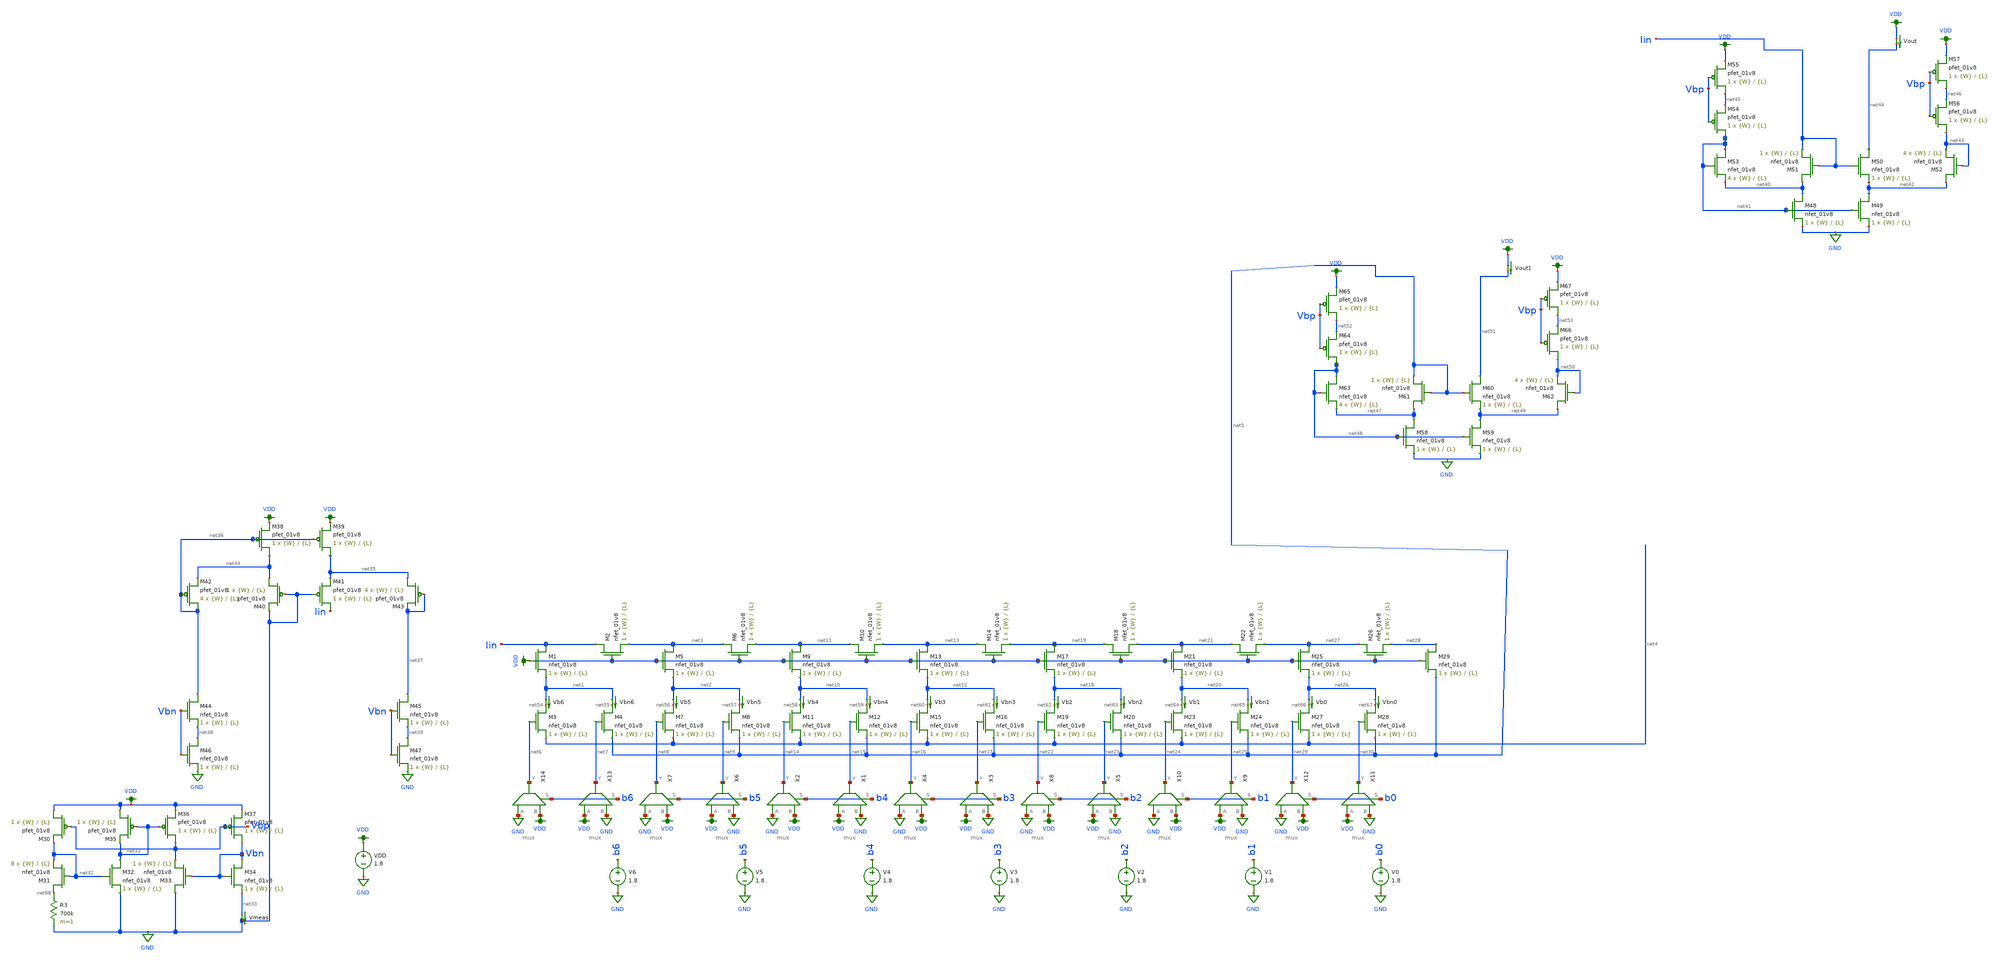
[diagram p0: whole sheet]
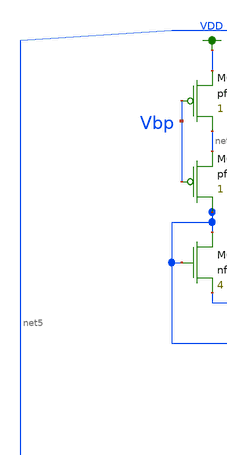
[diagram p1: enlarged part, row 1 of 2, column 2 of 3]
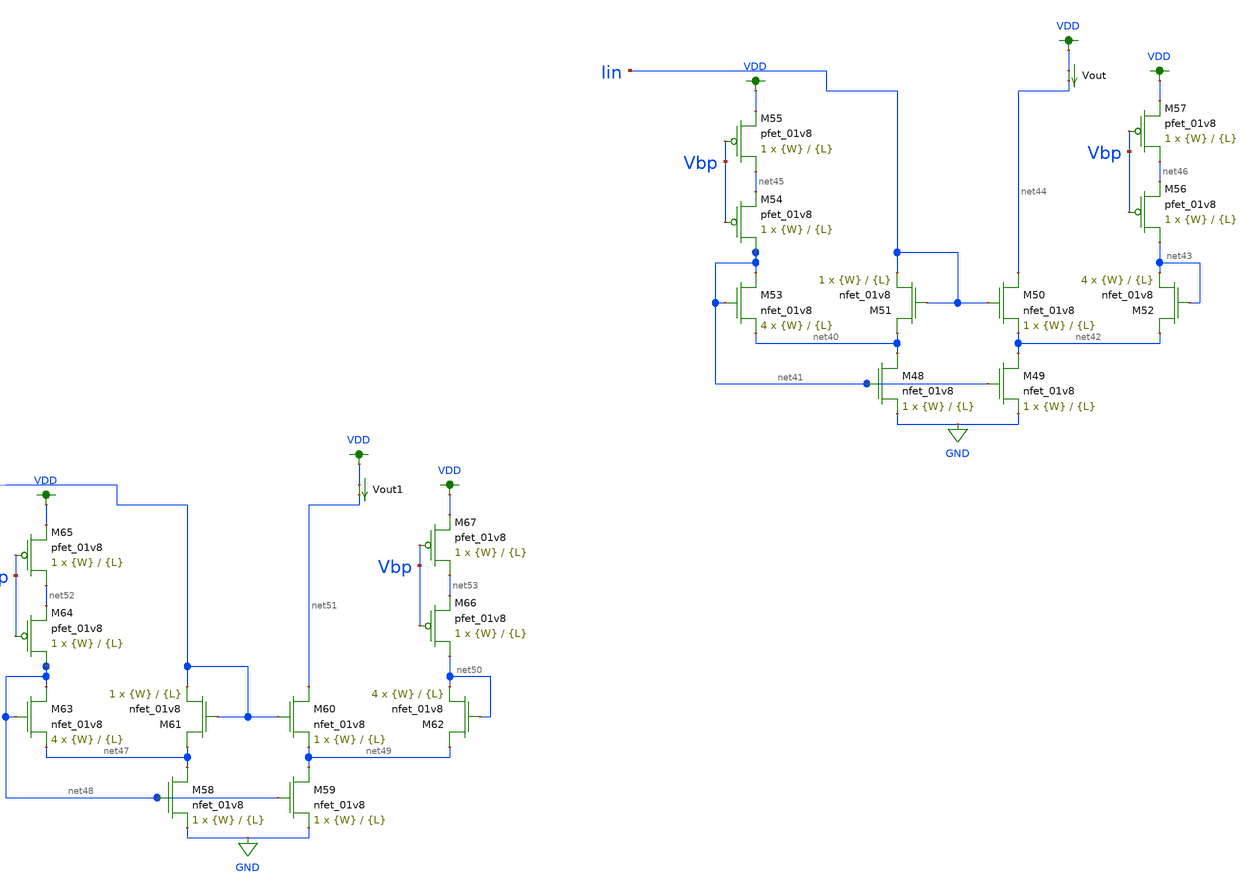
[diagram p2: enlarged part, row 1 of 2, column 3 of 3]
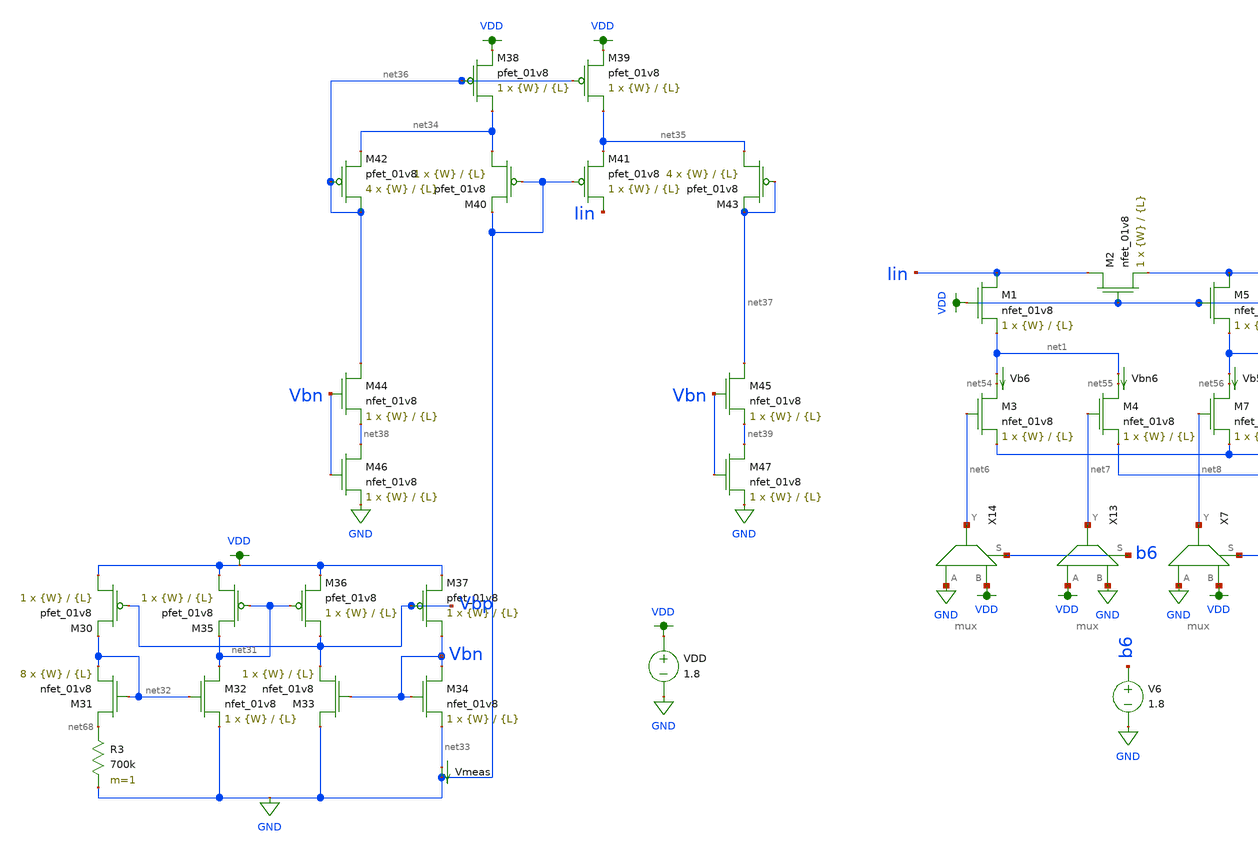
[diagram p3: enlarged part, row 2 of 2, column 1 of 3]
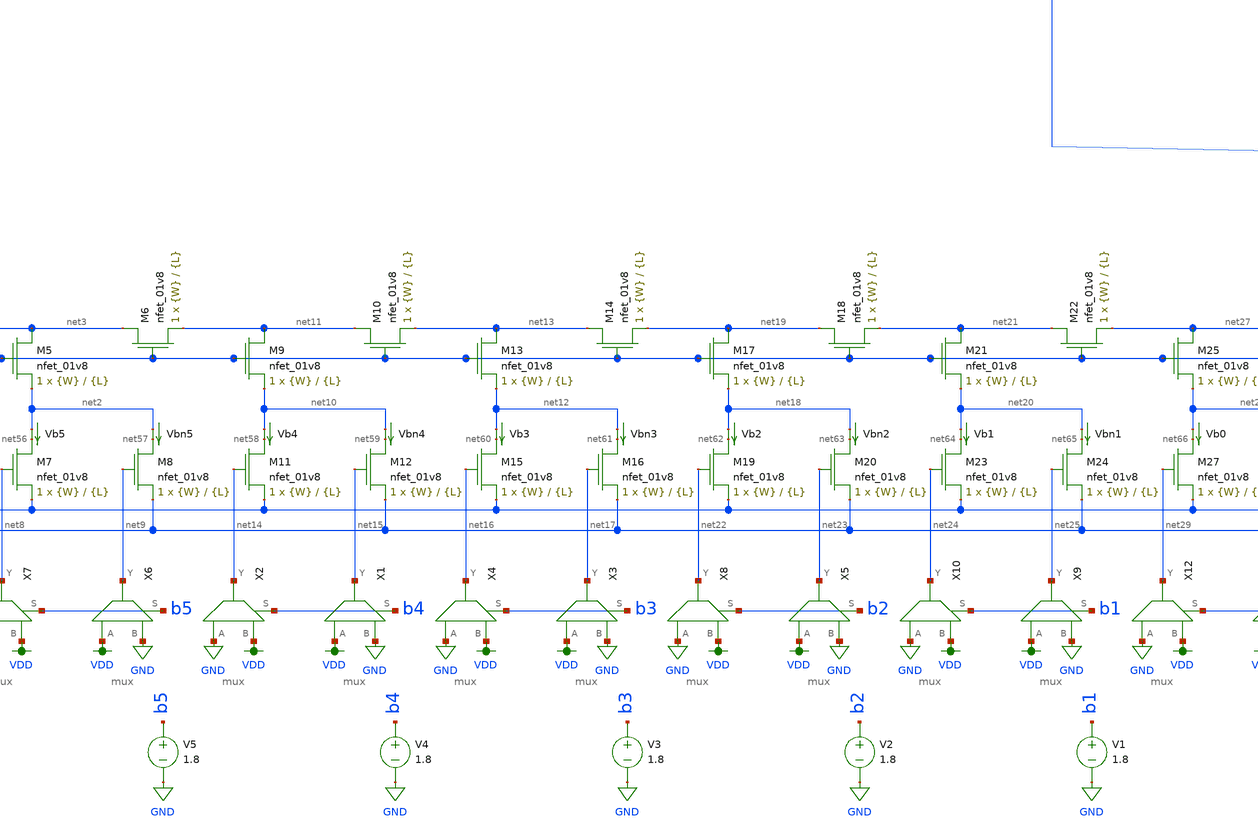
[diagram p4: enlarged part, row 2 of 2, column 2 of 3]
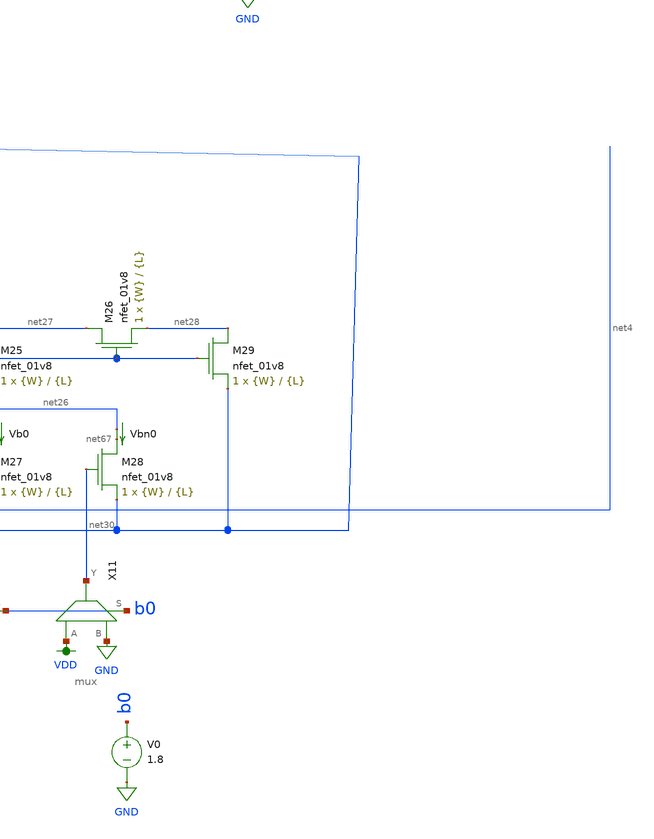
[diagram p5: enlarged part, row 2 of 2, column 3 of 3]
** sch_path: dac/schematics/misc/dac_from_paper_3.sch
**.subckt dac_from_paper_3
XM1 Iin VDD net1 GND sky130_fd_pr__nfet_01v8 L={L} W={W} nf=1 ad='int((nf+1)/2) * W/nf * 0.29' as='int((nf+2)/2) * W/nf * 0.29'
+ pd='2*int((nf+1)/2) * (W/nf + 0.29)' ps='2*int((nf+2)/2) * (W/nf + 0.29)' nrd='0.29 / W' nrs='0.29 / W'
+ sa=0 sb=0 sd=0 mult=1 m=1
XM2 Iin VDD net3 GND sky130_fd_pr__nfet_01v8 L={L} W={W} nf=1 ad='int((nf+1)/2) * W/nf * 0.29' as='int((nf+2)/2) * W/nf * 0.29'
+ pd='2*int((nf+1)/2) * (W/nf + 0.29)' ps='2*int((nf+2)/2) * (W/nf + 0.29)' nrd='0.29 / W' nrs='0.29 / W'
+ sa=0 sb=0 sd=0 mult=1 m=1
XM3 net54 net6 net4 GND sky130_fd_pr__nfet_01v8 L={L} W={W} nf=1 ad='int((nf+1)/2) * W/nf * 0.29' as='int((nf+2)/2) * W/nf * 0.29'
+ pd='2*int((nf+1)/2) * (W/nf + 0.29)' ps='2*int((nf+2)/2) * (W/nf + 0.29)' nrd='0.29 / W' nrs='0.29 / W'
+ sa=0 sb=0 sd=0 mult=1 m=1
XM4 net55 net7 net5 GND sky130_fd_pr__nfet_01v8 L={L} W={W} nf=1 ad='int((nf+1)/2) * W/nf * 0.29' as='int((nf+2)/2) * W/nf * 0.29'
+ pd='2*int((nf+1)/2) * (W/nf + 0.29)' ps='2*int((nf+2)/2) * (W/nf + 0.29)' nrd='0.29 / W' nrs='0.29 / W'
+ sa=0 sb=0 sd=0 mult=1 m=1
XM5 net3 VDD net2 GND sky130_fd_pr__nfet_01v8 L={L} W={W} nf=1 ad='int((nf+1)/2) * W/nf * 0.29' as='int((nf+2)/2) * W/nf * 0.29'
+ pd='2*int((nf+1)/2) * (W/nf + 0.29)' ps='2*int((nf+2)/2) * (W/nf + 0.29)' nrd='0.29 / W' nrs='0.29 / W'
+ sa=0 sb=0 sd=0 mult=1 m=1
XM6 net3 VDD net11 GND sky130_fd_pr__nfet_01v8 L={L} W={W} nf=1 ad='int((nf+1)/2) * W/nf * 0.29' as='int((nf+2)/2) * W/nf * 0.29'
+ pd='2*int((nf+1)/2) * (W/nf + 0.29)' ps='2*int((nf+2)/2) * (W/nf + 0.29)' nrd='0.29 / W' nrs='0.29 / W'
+ sa=0 sb=0 sd=0 mult=1 m=1
XM7 net56 net8 net4 GND sky130_fd_pr__nfet_01v8 L={L} W={W} nf=1 ad='int((nf+1)/2) * W/nf * 0.29' as='int((nf+2)/2) * W/nf * 0.29'
+ pd='2*int((nf+1)/2) * (W/nf + 0.29)' ps='2*int((nf+2)/2) * (W/nf + 0.29)' nrd='0.29 / W' nrs='0.29 / W'
+ sa=0 sb=0 sd=0 mult=1 m=1
XM8 net57 net9 net5 GND sky130_fd_pr__nfet_01v8 L={L} W={W} nf=1 ad='int((nf+1)/2) * W/nf * 0.29' as='int((nf+2)/2) * W/nf * 0.29'
+ pd='2*int((nf+1)/2) * (W/nf + 0.29)' ps='2*int((nf+2)/2) * (W/nf + 0.29)' nrd='0.29 / W' nrs='0.29 / W'
+ sa=0 sb=0 sd=0 mult=1 m=1
XM9 net11 VDD net10 GND sky130_fd_pr__nfet_01v8 L={L} W={W} nf=1 ad='int((nf+1)/2) * W/nf * 0.29' as='int((nf+2)/2) * W/nf * 0.29'
+ pd='2*int((nf+1)/2) * (W/nf + 0.29)' ps='2*int((nf+2)/2) * (W/nf + 0.29)' nrd='0.29 / W' nrs='0.29 / W'
+ sa=0 sb=0 sd=0 mult=1 m=1
XM10 net11 VDD net13 GND sky130_fd_pr__nfet_01v8 L={L} W={W} nf=1 ad='int((nf+1)/2) * W/nf * 0.29' as='int((nf+2)/2) * W/nf * 0.29'
+ pd='2*int((nf+1)/2) * (W/nf + 0.29)' ps='2*int((nf+2)/2) * (W/nf + 0.29)' nrd='0.29 / W' nrs='0.29 / W'
+ sa=0 sb=0 sd=0 mult=1 m=1
XM11 net58 net14 net4 GND sky130_fd_pr__nfet_01v8 L={L} W={W} nf=1 ad='int((nf+1)/2) * W/nf * 0.29' as='int((nf+2)/2) * W/nf * 0.29'
+ pd='2*int((nf+1)/2) * (W/nf + 0.29)' ps='2*int((nf+2)/2) * (W/nf + 0.29)' nrd='0.29 / W' nrs='0.29 / W'
+ sa=0 sb=0 sd=0 mult=1 m=1
XM12 net59 net15 net5 GND sky130_fd_pr__nfet_01v8 L={L} W={W} nf=1 ad='int((nf+1)/2) * W/nf * 0.29' as='int((nf+2)/2) * W/nf * 0.29'
+ pd='2*int((nf+1)/2) * (W/nf + 0.29)' ps='2*int((nf+2)/2) * (W/nf + 0.29)' nrd='0.29 / W' nrs='0.29 / W'
+ sa=0 sb=0 sd=0 mult=1 m=1
XM13 net13 VDD net12 GND sky130_fd_pr__nfet_01v8 L={L} W={W} nf=1 ad='int((nf+1)/2) * W/nf * 0.29' as='int((nf+2)/2) * W/nf * 0.29'
+ pd='2*int((nf+1)/2) * (W/nf + 0.29)' ps='2*int((nf+2)/2) * (W/nf + 0.29)' nrd='0.29 / W' nrs='0.29 / W'
+ sa=0 sb=0 sd=0 mult=1 m=1
XM14 net13 VDD net19 GND sky130_fd_pr__nfet_01v8 L={L} W={W} nf=1 ad='int((nf+1)/2) * W/nf * 0.29' as='int((nf+2)/2) * W/nf * 0.29'
+ pd='2*int((nf+1)/2) * (W/nf + 0.29)' ps='2*int((nf+2)/2) * (W/nf + 0.29)' nrd='0.29 / W' nrs='0.29 / W'
+ sa=0 sb=0 sd=0 mult=1 m=1
XM15 net60 net16 net4 GND sky130_fd_pr__nfet_01v8 L={L} W={W} nf=1 ad='int((nf+1)/2) * W/nf * 0.29' as='int((nf+2)/2) * W/nf * 0.29'
+ pd='2*int((nf+1)/2) * (W/nf + 0.29)' ps='2*int((nf+2)/2) * (W/nf + 0.29)' nrd='0.29 / W' nrs='0.29 / W'
+ sa=0 sb=0 sd=0 mult=1 m=1
XM16 net61 net17 net5 GND sky130_fd_pr__nfet_01v8 L={L} W={W} nf=1 ad='int((nf+1)/2) * W/nf * 0.29' as='int((nf+2)/2) * W/nf * 0.29'
+ pd='2*int((nf+1)/2) * (W/nf + 0.29)' ps='2*int((nf+2)/2) * (W/nf + 0.29)' nrd='0.29 / W' nrs='0.29 / W'
+ sa=0 sb=0 sd=0 mult=1 m=1
XM17 net19 VDD net18 GND sky130_fd_pr__nfet_01v8 L={L} W={W} nf=1 ad='int((nf+1)/2) * W/nf * 0.29' as='int((nf+2)/2) * W/nf * 0.29'
+ pd='2*int((nf+1)/2) * (W/nf + 0.29)' ps='2*int((nf+2)/2) * (W/nf + 0.29)' nrd='0.29 / W' nrs='0.29 / W'
+ sa=0 sb=0 sd=0 mult=1 m=1
XM18 net19 VDD net21 GND sky130_fd_pr__nfet_01v8 L={L} W={W} nf=1 ad='int((nf+1)/2) * W/nf * 0.29' as='int((nf+2)/2) * W/nf * 0.29'
+ pd='2*int((nf+1)/2) * (W/nf + 0.29)' ps='2*int((nf+2)/2) * (W/nf + 0.29)' nrd='0.29 / W' nrs='0.29 / W'
+ sa=0 sb=0 sd=0 mult=1 m=1
XM19 net62 net22 net4 GND sky130_fd_pr__nfet_01v8 L={L} W={W} nf=1 ad='int((nf+1)/2) * W/nf * 0.29' as='int((nf+2)/2) * W/nf * 0.29'
+ pd='2*int((nf+1)/2) * (W/nf + 0.29)' ps='2*int((nf+2)/2) * (W/nf + 0.29)' nrd='0.29 / W' nrs='0.29 / W'
+ sa=0 sb=0 sd=0 mult=1 m=1
XM20 net63 net23 net5 GND sky130_fd_pr__nfet_01v8 L={L} W={W} nf=1 ad='int((nf+1)/2) * W/nf * 0.29' as='int((nf+2)/2) * W/nf * 0.29'
+ pd='2*int((nf+1)/2) * (W/nf + 0.29)' ps='2*int((nf+2)/2) * (W/nf + 0.29)' nrd='0.29 / W' nrs='0.29 / W'
+ sa=0 sb=0 sd=0 mult=1 m=1
XM21 net21 VDD net20 GND sky130_fd_pr__nfet_01v8 L={L} W={W} nf=1 ad='int((nf+1)/2) * W/nf * 0.29' as='int((nf+2)/2) * W/nf * 0.29'
+ pd='2*int((nf+1)/2) * (W/nf + 0.29)' ps='2*int((nf+2)/2) * (W/nf + 0.29)' nrd='0.29 / W' nrs='0.29 / W'
+ sa=0 sb=0 sd=0 mult=1 m=1
XM22 net21 VDD net27 GND sky130_fd_pr__nfet_01v8 L={L} W={W} nf=1 ad='int((nf+1)/2) * W/nf * 0.29' as='int((nf+2)/2) * W/nf * 0.29'
+ pd='2*int((nf+1)/2) * (W/nf + 0.29)' ps='2*int((nf+2)/2) * (W/nf + 0.29)' nrd='0.29 / W' nrs='0.29 / W'
+ sa=0 sb=0 sd=0 mult=1 m=1
XM23 net64 net24 net4 GND sky130_fd_pr__nfet_01v8 L={L} W={W} nf=1 ad='int((nf+1)/2) * W/nf * 0.29' as='int((nf+2)/2) * W/nf * 0.29'
+ pd='2*int((nf+1)/2) * (W/nf + 0.29)' ps='2*int((nf+2)/2) * (W/nf + 0.29)' nrd='0.29 / W' nrs='0.29 / W'
+ sa=0 sb=0 sd=0 mult=1 m=1
XM24 net65 net25 net5 GND sky130_fd_pr__nfet_01v8 L={L} W={W} nf=1 ad='int((nf+1)/2) * W/nf * 0.29' as='int((nf+2)/2) * W/nf * 0.29'
+ pd='2*int((nf+1)/2) * (W/nf + 0.29)' ps='2*int((nf+2)/2) * (W/nf + 0.29)' nrd='0.29 / W' nrs='0.29 / W'
+ sa=0 sb=0 sd=0 mult=1 m=1
XM25 net27 VDD net26 GND sky130_fd_pr__nfet_01v8 L={L} W={W} nf=1 ad='int((nf+1)/2) * W/nf * 0.29' as='int((nf+2)/2) * W/nf * 0.29'
+ pd='2*int((nf+1)/2) * (W/nf + 0.29)' ps='2*int((nf+2)/2) * (W/nf + 0.29)' nrd='0.29 / W' nrs='0.29 / W'
+ sa=0 sb=0 sd=0 mult=1 m=1
XM26 net27 VDD net28 GND sky130_fd_pr__nfet_01v8 L={L} W={W} nf=1 ad='int((nf+1)/2) * W/nf * 0.29' as='int((nf+2)/2) * W/nf * 0.29'
+ pd='2*int((nf+1)/2) * (W/nf + 0.29)' ps='2*int((nf+2)/2) * (W/nf + 0.29)' nrd='0.29 / W' nrs='0.29 / W'
+ sa=0 sb=0 sd=0 mult=1 m=1
XM27 net66 net29 net4 GND sky130_fd_pr__nfet_01v8 L={L} W={W} nf=1 ad='int((nf+1)/2) * W/nf * 0.29' as='int((nf+2)/2) * W/nf * 0.29'
+ pd='2*int((nf+1)/2) * (W/nf + 0.29)' ps='2*int((nf+2)/2) * (W/nf + 0.29)' nrd='0.29 / W' nrs='0.29 / W'
+ sa=0 sb=0 sd=0 mult=1 m=1
XM28 net67 net30 net5 GND sky130_fd_pr__nfet_01v8 L={L} W={W} nf=1 ad='int((nf+1)/2) * W/nf * 0.29' as='int((nf+2)/2) * W/nf * 0.29'
+ pd='2*int((nf+1)/2) * (W/nf + 0.29)' ps='2*int((nf+2)/2) * (W/nf + 0.29)' nrd='0.29 / W' nrs='0.29 / W'
+ sa=0 sb=0 sd=0 mult=1 m=1
XM29 net28 VDD net5 GND sky130_fd_pr__nfet_01v8 L={L} W={W} nf=1 ad='int((nf+1)/2) * W/nf * 0.29' as='int((nf+2)/2) * W/nf * 0.29'
+ pd='2*int((nf+1)/2) * (W/nf + 0.29)' ps='2*int((nf+2)/2) * (W/nf + 0.29)' nrd='0.29 / W' nrs='0.29 / W'
+ sa=0 sb=0 sd=0 mult=1 m=1
Vb0 net26 net66 0
.save i(vb0)
Vbn0 net26 net67 0
.save i(vbn0)
Vb5 net2 net56 0
.save i(vb5)
Vb6 net1 net54 0
.save i(vb6)
Vb1 net20 net64 0
.save i(vb1)
Vb2 net18 net62 0
.save i(vb2)
Vb3 net12 net60 0
.save i(vb3)
Vb4 net10 net58 0
.save i(vb4)
Vbn1 net20 net65 0
.save i(vbn1)
Vbn2 net18 net63 0
.save i(vbn2)
Vbn3 net12 net61 0
.save i(vbn3)
Vbn4 net10 net59 0
.save i(vbn4)
Vbn5 net2 net57 0
.save i(vbn5)
Vbn6 net1 net55 0
.save i(vbn6)
V0 b0 GND 1.8
V1 b1 GND 1.8
V2 b2 GND 1.8
V3 b3 GND 1.8
V4 b4 GND 1.8
V5 b5 GND 1.8
V6 b6 GND 1.8
XM30 VDD Vbp net32 VDD sky130_fd_pr__pfet_01v8 L={L} W={W} nf=1 ad='int((nf+1)/2) * W/nf * 0.29' as='int((nf+2)/2) * W/nf * 0.29'
+ pd='2*int((nf+1)/2) * (W/nf + 0.29)' ps='2*int((nf+2)/2) * (W/nf + 0.29)' nrd='0.29 / W' nrs='0.29 / W'
+ sa=0 sb=0 sd=0 mult=1 m=1
XM31 net68 net32 net32 GND sky130_fd_pr__nfet_01v8 L={L} W={W} nf=1 ad='int((nf+1)/2) * W/nf * 0.29'
+ as='int((nf+2)/2) * W/nf * 0.29' pd='2*int((nf+1)/2) * (W/nf + 0.29)' ps='2*int((nf+2)/2) * (W/nf + 0.29)'
+ nrd='0.29 / W' nrs='0.29 / W' sa=0 sb=0 sd=0 mult=8 m=8
R3 net68 GND 700k m=1
XM32 net31 net32 GND GND sky130_fd_pr__nfet_01v8 L={L} W={W} nf=1 ad='int((nf+1)/2) * W/nf * 0.29' as='int((nf+2)/2) * W/nf * 0.29'
+ pd='2*int((nf+1)/2) * (W/nf + 0.29)' ps='2*int((nf+2)/2) * (W/nf + 0.29)' nrd='0.29 / W' nrs='0.29 / W'
+ sa=0 sb=0 sd=0 mult=1 m=1
XM33 GND Vbn Vbp GND sky130_fd_pr__nfet_01v8 L={L} W={W} nf=1 ad='int((nf+1)/2) * W/nf * 0.29' as='int((nf+2)/2) * W/nf * 0.29'
+ pd='2*int((nf+1)/2) * (W/nf + 0.29)' ps='2*int((nf+2)/2) * (W/nf + 0.29)' nrd='0.29 / W' nrs='0.29 / W'
+ sa=0 sb=0 sd=0 mult=1 m=1
XM34 Vbn Vbn net33 GND sky130_fd_pr__nfet_01v8 L={L} W={W} nf=1 ad='int((nf+1)/2) * W/nf * 0.29' as='int((nf+2)/2) * W/nf * 0.29'
+ pd='2*int((nf+1)/2) * (W/nf + 0.29)' ps='2*int((nf+2)/2) * (W/nf + 0.29)' nrd='0.29 / W' nrs='0.29 / W'
+ sa=0 sb=0 sd=0 mult=1 m=1
XM35 VDD net31 net31 VDD sky130_fd_pr__pfet_01v8 L={L} W={W} nf=1 ad='int((nf+1)/2) * W/nf * 0.29' as='int((nf+2)/2) * W/nf * 0.29'
+ pd='2*int((nf+1)/2) * (W/nf + 0.29)' ps='2*int((nf+2)/2) * (W/nf + 0.29)' nrd='0.29 / W' nrs='0.29 / W'
+ sa=0 sb=0 sd=0 mult=1 m=1
XM36 Vbp net31 VDD VDD sky130_fd_pr__pfet_01v8 L={L} W={W} nf=1 ad='int((nf+1)/2) * W/nf * 0.29' as='int((nf+2)/2) * W/nf * 0.29'
+ pd='2*int((nf+1)/2) * (W/nf + 0.29)' ps='2*int((nf+2)/2) * (W/nf + 0.29)' nrd='0.29 / W' nrs='0.29 / W'
+ sa=0 sb=0 sd=0 mult=1 m=1
XM37 Vbn Vbp VDD VDD sky130_fd_pr__pfet_01v8 L={L} W={W} nf=1 ad='int((nf+1)/2) * W/nf * 0.29' as='int((nf+2)/2) * W/nf * 0.29'
+ pd='2*int((nf+1)/2) * (W/nf + 0.29)' ps='2*int((nf+2)/2) * (W/nf + 0.29)' nrd='0.29 / W' nrs='0.29 / W'
+ sa=0 sb=0 sd=0 mult=1 m=1
VDD VDD GND 1.8
Vmeas net33 GND 0
.save i(vmeas)
X13 VDD GND net7 b6 mux
X14 GND VDD net6 b6 mux
X6 VDD GND net9 b5 mux
X7 GND VDD net8 b5 mux
X1 VDD GND net15 b4 mux
X2 GND VDD net14 b4 mux
X3 VDD GND net17 b3 mux
X4 GND VDD net16 b3 mux
X5 VDD GND net23 b2 mux
X8 GND VDD net22 b2 mux
X9 VDD GND net25 b1 mux
X10 GND VDD net24 b1 mux
X11 VDD GND net30 b0 mux
X12 GND VDD net29 b0 mux
XM38 net34 net36 VDD VDD sky130_fd_pr__pfet_01v8 L={L} W={W} nf=1 ad='int((nf+1)/2) * W/nf * 0.29' as='int((nf+2)/2) * W/nf * 0.29'
+ pd='2*int((nf+1)/2) * (W/nf + 0.29)' ps='2*int((nf+2)/2) * (W/nf + 0.29)' nrd='0.29 / W' nrs='0.29 / W'
+ sa=0 sb=0 sd=0 mult=1 m=1
XM39 net35 net36 VDD VDD sky130_fd_pr__pfet_01v8 L={L} W={W} nf=1 ad='int((nf+1)/2) * W/nf * 0.29' as='int((nf+2)/2) * W/nf * 0.29'
+ pd='2*int((nf+1)/2) * (W/nf + 0.29)' ps='2*int((nf+2)/2) * (W/nf + 0.29)' nrd='0.29 / W' nrs='0.29 / W'
+ sa=0 sb=0 sd=0 mult=1 m=1
XM40 net34 GND GND VDD sky130_fd_pr__pfet_01v8 L={L} W={W} nf=1 ad='int((nf+1)/2) * W/nf * 0.29' as='int((nf+2)/2) * W/nf * 0.29'
+ pd='2*int((nf+1)/2) * (W/nf + 0.29)' ps='2*int((nf+2)/2) * (W/nf + 0.29)' nrd='0.29 / W' nrs='0.29 / W'
+ sa=0 sb=0 sd=0 mult=1 m=1
XM41 Iin GND net35 VDD sky130_fd_pr__pfet_01v8 L={L} W={W} nf=1 ad='int((nf+1)/2) * W/nf * 0.29' as='int((nf+2)/2) * W/nf * 0.29'
+ pd='2*int((nf+1)/2) * (W/nf + 0.29)' ps='2*int((nf+2)/2) * (W/nf + 0.29)' nrd='0.29 / W' nrs='0.29 / W'
+ sa=0 sb=0 sd=0 mult=1 m=1
XM42 net36 net36 net34 VDD sky130_fd_pr__pfet_01v8 L={L} W={W} nf=1 ad='int((nf+1)/2) * W/nf * 0.29'
+ as='int((nf+2)/2) * W/nf * 0.29' pd='2*int((nf+1)/2) * (W/nf + 0.29)' ps='2*int((nf+2)/2) * (W/nf + 0.29)'
+ nrd='0.29 / W' nrs='0.29 / W' sa=0 sb=0 sd=0 mult=4 m=4
XM43 net35 net37 net37 VDD sky130_fd_pr__pfet_01v8 L={L} W={W} nf=1 ad='int((nf+1)/2) * W/nf * 0.29'
+ as='int((nf+2)/2) * W/nf * 0.29' pd='2*int((nf+1)/2) * (W/nf + 0.29)' ps='2*int((nf+2)/2) * (W/nf + 0.29)'
+ nrd='0.29 / W' nrs='0.29 / W' sa=0 sb=0 sd=0 mult=4 m=4
XM44 net36 Vbn net38 GND sky130_fd_pr__nfet_01v8 L={L} W={W} nf=1 ad='int((nf+1)/2) * W/nf * 0.29' as='int((nf+2)/2) * W/nf * 0.29'
+ pd='2*int((nf+1)/2) * (W/nf + 0.29)' ps='2*int((nf+2)/2) * (W/nf + 0.29)' nrd='0.29 / W' nrs='0.29 / W'
+ sa=0 sb=0 sd=0 mult=1 m=1
XM45 net37 Vbn net39 GND sky130_fd_pr__nfet_01v8 L={L} W={W} nf=1 ad='int((nf+1)/2) * W/nf * 0.29' as='int((nf+2)/2) * W/nf * 0.29'
+ pd='2*int((nf+1)/2) * (W/nf + 0.29)' ps='2*int((nf+2)/2) * (W/nf + 0.29)' nrd='0.29 / W' nrs='0.29 / W'
+ sa=0 sb=0 sd=0 mult=1 m=1
XM46 net38 Vbn GND GND sky130_fd_pr__nfet_01v8 L={L} W={W} nf=1 ad='int((nf+1)/2) * W/nf * 0.29' as='int((nf+2)/2) * W/nf * 0.29'
+ pd='2*int((nf+1)/2) * (W/nf + 0.29)' ps='2*int((nf+2)/2) * (W/nf + 0.29)' nrd='0.29 / W' nrs='0.29 / W'
+ sa=0 sb=0 sd=0 mult=1 m=1
XM47 net39 Vbn GND GND sky130_fd_pr__nfet_01v8 L={L} W={W} nf=1 ad='int((nf+1)/2) * W/nf * 0.29' as='int((nf+2)/2) * W/nf * 0.29'
+ pd='2*int((nf+1)/2) * (W/nf + 0.29)' ps='2*int((nf+2)/2) * (W/nf + 0.29)' nrd='0.29 / W' nrs='0.29 / W'
+ sa=0 sb=0 sd=0 mult=1 m=1
XM48 net40 net41 GND GND sky130_fd_pr__nfet_01v8 L={L} W={W} nf=1 ad='int((nf+1)/2) * W/nf * 0.29' as='int((nf+2)/2) * W/nf * 0.29'
+ pd='2*int((nf+1)/2) * (W/nf + 0.29)' ps='2*int((nf+2)/2) * (W/nf + 0.29)' nrd='0.29 / W' nrs='0.29 / W'
+ sa=0 sb=0 sd=0 mult=1 m=1
XM49 net42 net41 GND GND sky130_fd_pr__nfet_01v8 L={L} W={W} nf=1 ad='int((nf+1)/2) * W/nf * 0.29' as='int((nf+2)/2) * W/nf * 0.29'
+ pd='2*int((nf+1)/2) * (W/nf + 0.29)' ps='2*int((nf+2)/2) * (W/nf + 0.29)' nrd='0.29 / W' nrs='0.29 / W'
+ sa=0 sb=0 sd=0 mult=1 m=1
XM50 net44 Iin net42 GND sky130_fd_pr__nfet_01v8 L={L} W={W} nf=1 ad='int((nf+1)/2) * W/nf * 0.29' as='int((nf+2)/2) * W/nf * 0.29'
+ pd='2*int((nf+1)/2) * (W/nf + 0.29)' ps='2*int((nf+2)/2) * (W/nf + 0.29)' nrd='0.29 / W' nrs='0.29 / W'
+ sa=0 sb=0 sd=0 mult=1 m=1
XM51 net40 Iin Iin GND sky130_fd_pr__nfet_01v8 L={L} W={W} nf=1 ad='int((nf+1)/2) * W/nf * 0.29' as='int((nf+2)/2) * W/nf * 0.29'
+ pd='2*int((nf+1)/2) * (W/nf + 0.29)' ps='2*int((nf+2)/2) * (W/nf + 0.29)' nrd='0.29 / W' nrs='0.29 / W'
+ sa=0 sb=0 sd=0 mult=1 m=1
XM52 net42 net43 net43 GND sky130_fd_pr__nfet_01v8 L={L} W={W} nf=1 ad='int((nf+1)/2) * W/nf * 0.29'
+ as='int((nf+2)/2) * W/nf * 0.29' pd='2*int((nf+1)/2) * (W/nf + 0.29)' ps='2*int((nf+2)/2) * (W/nf + 0.29)'
+ nrd='0.29 / W' nrs='0.29 / W' sa=0 sb=0 sd=0 mult=4 m=4
XM53 net41 net41 net40 GND sky130_fd_pr__nfet_01v8 L={L} W={W} nf=1 ad='int((nf+1)/2) * W/nf * 0.29'
+ as='int((nf+2)/2) * W/nf * 0.29' pd='2*int((nf+1)/2) * (W/nf + 0.29)' ps='2*int((nf+2)/2) * (W/nf + 0.29)'
+ nrd='0.29 / W' nrs='0.29 / W' sa=0 sb=0 sd=0 mult=4 m=4
XM54 net41 Vbp net45 VDD sky130_fd_pr__pfet_01v8 L={L} W={W} nf=1 ad='int((nf+1)/2) * W/nf * 0.29' as='int((nf+2)/2) * W/nf * 0.29'
+ pd='2*int((nf+1)/2) * (W/nf + 0.29)' ps='2*int((nf+2)/2) * (W/nf + 0.29)' nrd='0.29 / W' nrs='0.29 / W'
+ sa=0 sb=0 sd=0 mult=1 m=1
XM55 net45 Vbp VDD VDD sky130_fd_pr__pfet_01v8 L={L} W={W} nf=1 ad='int((nf+1)/2) * W/nf * 0.29' as='int((nf+2)/2) * W/nf * 0.29'
+ pd='2*int((nf+1)/2) * (W/nf + 0.29)' ps='2*int((nf+2)/2) * (W/nf + 0.29)' nrd='0.29 / W' nrs='0.29 / W'
+ sa=0 sb=0 sd=0 mult=1 m=1
XM56 net43 Vbp net46 VDD sky130_fd_pr__pfet_01v8 L={L} W={W} nf=1 ad='int((nf+1)/2) * W/nf * 0.29' as='int((nf+2)/2) * W/nf * 0.29'
+ pd='2*int((nf+1)/2) * (W/nf + 0.29)' ps='2*int((nf+2)/2) * (W/nf + 0.29)' nrd='0.29 / W' nrs='0.29 / W'
+ sa=0 sb=0 sd=0 mult=1 m=1
XM57 net46 Vbp VDD VDD sky130_fd_pr__pfet_01v8 L={L} W={W} nf=1 ad='int((nf+1)/2) * W/nf * 0.29' as='int((nf+2)/2) * W/nf * 0.29'
+ pd='2*int((nf+1)/2) * (W/nf + 0.29)' ps='2*int((nf+2)/2) * (W/nf + 0.29)' nrd='0.29 / W' nrs='0.29 / W'
+ sa=0 sb=0 sd=0 mult=1 m=1
Vout VDD net44 0
.save i(vout)
XM58 net47 net48 GND GND sky130_fd_pr__nfet_01v8 L={L} W={W} nf=1 ad='int((nf+1)/2) * W/nf * 0.29' as='int((nf+2)/2) * W/nf * 0.29'
+ pd='2*int((nf+1)/2) * (W/nf + 0.29)' ps='2*int((nf+2)/2) * (W/nf + 0.29)' nrd='0.29 / W' nrs='0.29 / W'
+ sa=0 sb=0 sd=0 mult=1 m=1
XM59 net49 net48 GND GND sky130_fd_pr__nfet_01v8 L={L} W={W} nf=1 ad='int((nf+1)/2) * W/nf * 0.29' as='int((nf+2)/2) * W/nf * 0.29'
+ pd='2*int((nf+1)/2) * (W/nf + 0.29)' ps='2*int((nf+2)/2) * (W/nf + 0.29)' nrd='0.29 / W' nrs='0.29 / W'
+ sa=0 sb=0 sd=0 mult=1 m=1
XM60 net51 net5 net49 GND sky130_fd_pr__nfet_01v8 L={L} W={W} nf=1 ad='int((nf+1)/2) * W/nf * 0.29' as='int((nf+2)/2) * W/nf * 0.29'
+ pd='2*int((nf+1)/2) * (W/nf + 0.29)' ps='2*int((nf+2)/2) * (W/nf + 0.29)' nrd='0.29 / W' nrs='0.29 / W'
+ sa=0 sb=0 sd=0 mult=1 m=1
XM61 net47 net5 net5 GND sky130_fd_pr__nfet_01v8 L={L} W={W} nf=1 ad='int((nf+1)/2) * W/nf * 0.29' as='int((nf+2)/2) * W/nf * 0.29'
+ pd='2*int((nf+1)/2) * (W/nf + 0.29)' ps='2*int((nf+2)/2) * (W/nf + 0.29)' nrd='0.29 / W' nrs='0.29 / W'
+ sa=0 sb=0 sd=0 mult=1 m=1
XM62 net49 net50 net50 GND sky130_fd_pr__nfet_01v8 L={L} W={W} nf=1 ad='int((nf+1)/2) * W/nf * 0.29'
+ as='int((nf+2)/2) * W/nf * 0.29' pd='2*int((nf+1)/2) * (W/nf + 0.29)' ps='2*int((nf+2)/2) * (W/nf + 0.29)'
+ nrd='0.29 / W' nrs='0.29 / W' sa=0 sb=0 sd=0 mult=4 m=4
XM63 net48 net48 net47 GND sky130_fd_pr__nfet_01v8 L={L} W={W} nf=1 ad='int((nf+1)/2) * W/nf * 0.29'
+ as='int((nf+2)/2) * W/nf * 0.29' pd='2*int((nf+1)/2) * (W/nf + 0.29)' ps='2*int((nf+2)/2) * (W/nf + 0.29)'
+ nrd='0.29 / W' nrs='0.29 / W' sa=0 sb=0 sd=0 mult=4 m=4
XM64 net48 Vbp net52 VDD sky130_fd_pr__pfet_01v8 L={L} W={W} nf=1 ad='int((nf+1)/2) * W/nf * 0.29' as='int((nf+2)/2) * W/nf * 0.29'
+ pd='2*int((nf+1)/2) * (W/nf + 0.29)' ps='2*int((nf+2)/2) * (W/nf + 0.29)' nrd='0.29 / W' nrs='0.29 / W'
+ sa=0 sb=0 sd=0 mult=1 m=1
XM65 net52 Vbp VDD VDD sky130_fd_pr__pfet_01v8 L={L} W={W} nf=1 ad='int((nf+1)/2) * W/nf * 0.29' as='int((nf+2)/2) * W/nf * 0.29'
+ pd='2*int((nf+1)/2) * (W/nf + 0.29)' ps='2*int((nf+2)/2) * (W/nf + 0.29)' nrd='0.29 / W' nrs='0.29 / W'
+ sa=0 sb=0 sd=0 mult=1 m=1
XM66 net50 Vbp net53 VDD sky130_fd_pr__pfet_01v8 L={L} W={W} nf=1 ad='int((nf+1)/2) * W/nf * 0.29' as='int((nf+2)/2) * W/nf * 0.29'
+ pd='2*int((nf+1)/2) * (W/nf + 0.29)' ps='2*int((nf+2)/2) * (W/nf + 0.29)' nrd='0.29 / W' nrs='0.29 / W'
+ sa=0 sb=0 sd=0 mult=1 m=1
XM67 net53 Vbp VDD VDD sky130_fd_pr__pfet_01v8 L={L} W={W} nf=1 ad='int((nf+1)/2) * W/nf * 0.29' as='int((nf+2)/2) * W/nf * 0.29'
+ pd='2*int((nf+1)/2) * (W/nf + 0.29)' ps='2*int((nf+2)/2) * (W/nf + 0.29)' nrd='0.29 / W' nrs='0.29 / W'
+ sa=0 sb=0 sd=0 mult=1 m=1
Vout1 VDD net51 0
.save i(vout1)
**** begin user architecture code

.option wnflag=1
.param MC_SWITCH=0.0
.lib ~/skywater/skywater-pdk/libraries/sky130_fd_pr_ngspice/latest/models/sky130.lib.spice tt


.param W=64
.param L=8
.control
set wr_vecnames
set wr_singlescale
let code = 0
  while code < 128
    if code eq 0
      let b0 = 0
    else
      let b0 = code % 2
    end
    if floor(code / 2) eq 0
      let b1 = 0
    else
      let b1 = floor(code / 2) % 2
    end
    if floor(code / 4) eq 0
      let b2 = 0
    else
      let b2 = floor(code / 4) % 2
    end
    if floor(code / 8) eq 0
      let b3 = 0
    else
      let b3 = floor(code / 8) % 2
    end
    if floor(code / 16) eq 0
      let b4 = 0
    else
      let b4 = floor(code / 16) % 2
    end
    if floor(code / 32) eq 0
      let b5 = 0
    else
      let b5 = floor(code / 32) % 2
    end
    if floor(code / 64) eq 0
      let b6 = 0
    else
      let b6 = floor(code / 64) % 2
    end
    alter v0 $&b0
    alter v1 $&b1
    alter v2 $&b2
    alter v3 $&b3
    alter v4 $&b4
    alter v5 $&b5
    alter v6 $&b6
    save all
    op
    wrdata ~/Documents/current-output-dac-vlsi/simulations/dac_paper_sim.txt i(Vmeas) i(vb0) i(vb1)
+ i(vb2) i(vb3) i(vb4) i(vb5) i(vb6) i(Vout)
    if code eq 0
      set appendwrite
      set wr_vecnames = FALSE
    end
    let code = code + 1
  end
.endc

**** end user architecture code
**.ends

* expanding   symbol:  /home/madvlsi/Documents/current-output-dac-vlsi/schematics/mux.sym # of
*+ pins=4
** sym_path: dac/schematics/mux.sym
** sch_path: dac/schematics/mux.sch
.subckt mux A B Y S
*.ipin A
*.ipin B
*.ipin S
*.opin Y
XM1 A S Y VDD sky130_fd_pr__pfet_01v8 L=0.15 W=1 nf=1 ad='int((nf+1)/2) * W/nf * 0.29' as='int((nf+2)/2) * W/nf * 0.29'
+ pd='2*int((nf+1)/2) * (W/nf + 0.29)' ps='2*int((nf+2)/2) * (W/nf + 0.29)' nrd='0.29 / W' nrs='0.29 / W'
+ sa=0 sb=0 sd=0 mult=1 m=1
XM3 net1 S VDD VDD sky130_fd_pr__pfet_01v8 L=0.15 W=1 nf=1 ad='int((nf+1)/2) * W/nf * 0.29' as='int((nf+2)/2) * W/nf * 0.29'
+ pd='2*int((nf+1)/2) * (W/nf + 0.29)' ps='2*int((nf+2)/2) * (W/nf + 0.29)' nrd='0.29 / W' nrs='0.29 / W'
+ sa=0 sb=0 sd=0 mult=1 m=1
XM4 net1 S GND GND sky130_fd_pr__nfet_01v8 L=0.15 W=1 nf=1 ad='int((nf+1)/2) * W/nf * 0.29' as='int((nf+2)/2) * W/nf * 0.29'
+ pd='2*int((nf+1)/2) * (W/nf + 0.29)' ps='2*int((nf+2)/2) * (W/nf + 0.29)' nrd='0.29 / W' nrs='0.29 / W'
+ sa=0 sb=0 sd=0 mult=1 m=1
XM5 A net1 Y GND sky130_fd_pr__nfet_01v8 L=0.15 W=1 nf=1 ad='int((nf+1)/2) * W/nf * 0.29' as='int((nf+2)/2) * W/nf * 0.29'
+ pd='2*int((nf+1)/2) * (W/nf + 0.29)' ps='2*int((nf+2)/2) * (W/nf + 0.29)' nrd='0.29 / W' nrs='0.29 / W'
+ sa=0 sb=0 sd=0 mult=1 m=1
XM2 B net1 Y VDD sky130_fd_pr__pfet_01v8 L=0.15 W=1 nf=1 ad='int((nf+1)/2) * W/nf * 0.29' as='int((nf+2)/2) * W/nf * 0.29'
+ pd='2*int((nf+1)/2) * (W/nf + 0.29)' ps='2*int((nf+2)/2) * (W/nf + 0.29)' nrd='0.29 / W' nrs='0.29 / W'
+ sa=0 sb=0 sd=0 mult=1 m=1
XM6 B S Y GND sky130_fd_pr__nfet_01v8 L=0.15 W=1 nf=1 ad='int((nf+1)/2) * W/nf * 0.29' as='int((nf+2)/2) * W/nf * 0.29'
+ pd='2*int((nf+1)/2) * (W/nf + 0.29)' ps='2*int((nf+2)/2) * (W/nf + 0.29)' nrd='0.29 / W' nrs='0.29 / W'
+ sa=0 sb=0 sd=0 mult=1 m=1
.ends

.GLOBAL GND
.GLOBAL VDD
.end
